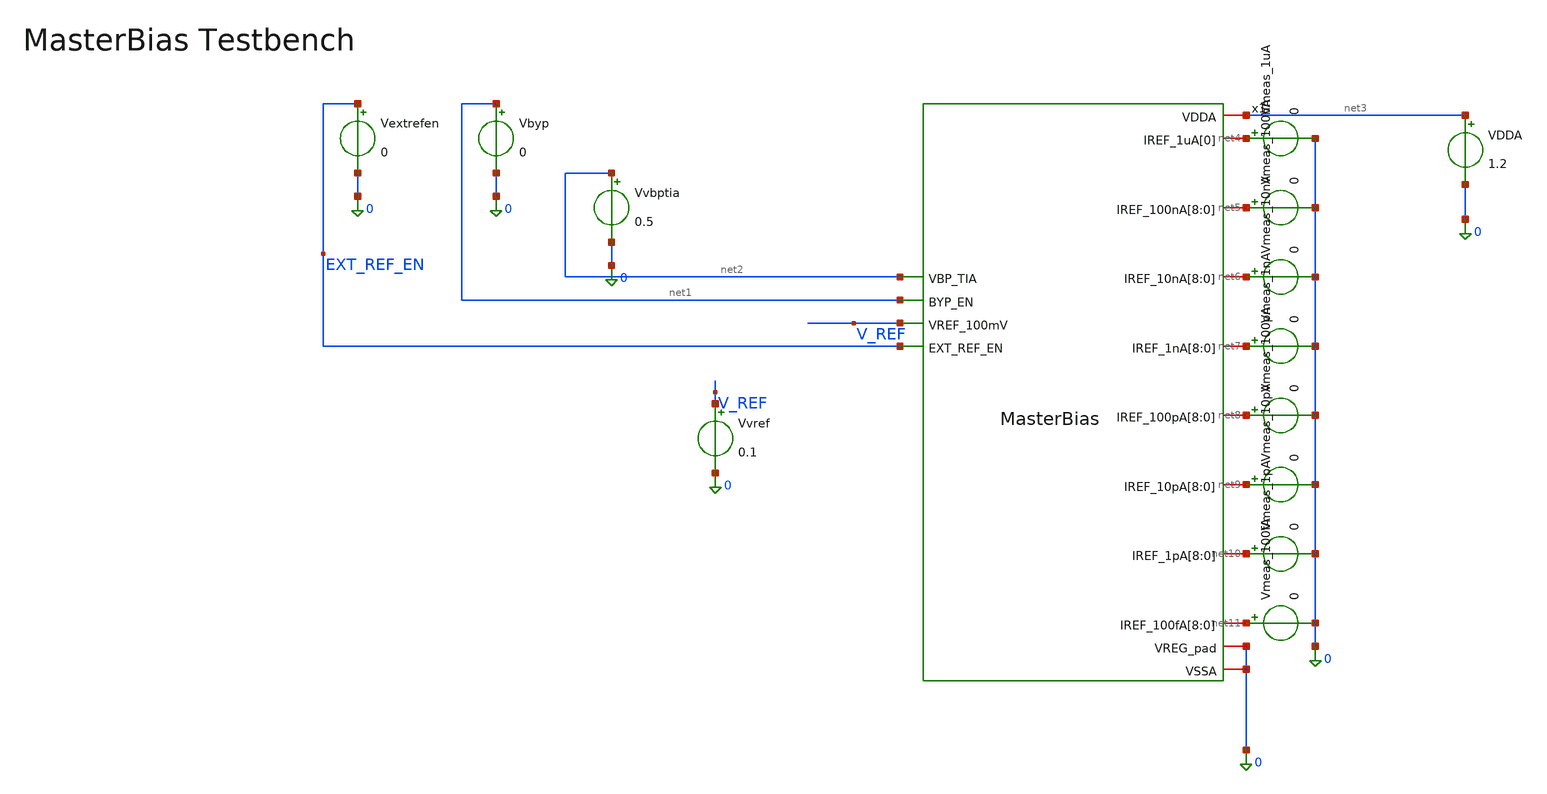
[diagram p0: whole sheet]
** sch_path: MasterBias_test.sch
**.subckt MasterBias_test
VDDA net3 0 1.2
Vmeas_1uA net4 0 0
.save i(vmeas_1ua)
Vmeas_100nA net5 0 0
.save i(vmeas_100na)
Vmeas_10nA net6 0 0
.save i(vmeas_10na)
Vmeas_1nA net7 0 0
.save i(vmeas_1na)
Vmeas_100pA net8 0 0
.save i(vmeas_100pa)
Vmeas_10pA net9 0 0
.save i(vmeas_10pa)
Vmeas_1pA net10 0 0
.save i(vmeas_1pa)
Vmeas_100fA net11 0 0
.save i(vmeas_100fa)
Vbyp net1 0 0
Vextrefen EXT_REF_EN 0 0
Vvbptia net2 0 0.5
Vvref V_REF 0 0.1
x1 net2 net1 V_REF EXT_REF_EN net3 net4 net5 net5 net5 net5 net5 net5 net5 net5 net5 net6 net6 net6
+ net6 net6 net6 net6 net6 net6 net7 net7 net7 net7 net7 net7 net7 net7 net7 net8 net8 net8 net8 net8 net8
+ net8 net8 net8 net9 net9 net9 net9 net9 net9 net9 net9 net9 net10 net10 net10 net10 net10 net10 net10
+ net10 net10 net11 net11 net11 net11 net11 net11 net11 net11 net11 0 0 MasterBias
**** begin user architecture code


.lib /foss/pdks/ihp-sg13cmos5l/libs.tech/ngspice/models/cornerMOSlv.lib mos_tt
.lib /foss/pdks/ihp-sg13cmos5l/libs.tech/ngspice/models/cornerMOShv.lib mos_tt
.include /foss/pdks/ihp-sg13cmos5l/libs.tech/ngspice/models/cap_mfringe.lib
.option savecurrents temp=27
.option abstol=1e-16
.option gmin=1e-16
* .nodeset hints for DC op (source-stepping often overrides these)
.nodeset v(x1.VBIAS)=0.5 v(x1.Vsense)=0.1 v(x1.x_ota.vout1stage)=0.7 v(x1.x_ota.vpmirr)=0.35
* .ic forces the UIC transient starting state
* vout1stage=0.7 puts M8 (HV NMOS) well above threshold so it can pull VBIAS down
.ic v(x1.VBIAS)=0.5 v(x1.Vsense)=0.05 v(x1.x_ota.vout1stage)=0.7 v(x1.x_ota.vpmirr)=0.35
+ v(x1.x1.Vbn)=0.4 v(x1.x2.Vbn)=0.4 v(x1.x3.Vbn)=0.4 v(x1.x4.Vbn)=0.4 v(x1.x5.Vbn)=0.4 v(x1.x6.Vbn)=0.4
+ v(x1.x7.Vbn)=0.4

.control
op

let cc = unitvec(8)
let cc[0] = abs(i(Vmeas_100fA))
let cc[1] = abs(i(Vmeas_1pA))
let cc[2] = abs(i(Vmeas_10pA))
let cc[3] = abs(i(Vmeas_100pA))
let cc[4] = abs(i(Vmeas_1nA))
let cc[5] = abs(i(Vmeas_10nA))
let cc[6] = abs(i(Vmeas_100nA))
let cc[7] = abs(i(Vmeas_1uA))

let Decade_Stage = unitvec(8)
let Decade_Stage[0] = 0
let Decade_Stage[1] = 1
let Decade_Stage[2] = 2
let Decade_Stage[3] = 3
let Decade_Stage[4] = 4
let Decade_Stage[5] = 5
let Decade_Stage[6] = 6
let Decade_Stage[7] = 7

let log10_I_A = log10(cc)

set title = Decade Division Linearity  [0=100fA  1=1pA  2=10pA  3=100pA  4=1nA  5=10nA  6=100nA
+  7=1uA]
plot log10_I_A vs Decade_Stage

print i(Vmeas_1uA) i(Vmeas_100nA) i(Vmeas_10nA) i(Vmeas_1nA)
print i(Vmeas_100pA) i(Vmeas_10pA) i(Vmeas_1pA) i(Vmeas_100fA)
write masterbias_op.raw

tran 1u 5m uic
write masterbias_tran.raw
.endc




**** end user architecture code
**.ends
.end
